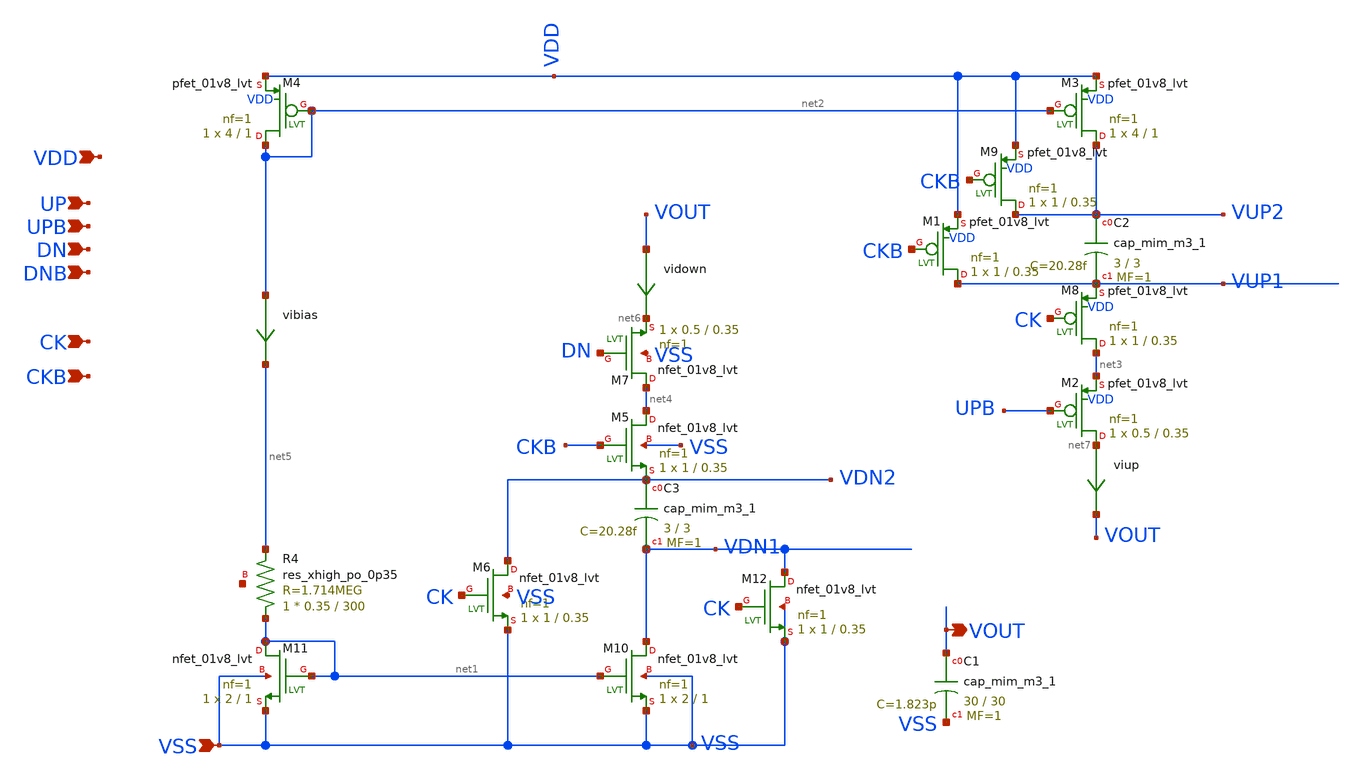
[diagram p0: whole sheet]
** sch_path: xschem/pll_cp_charlie.sch
**.subckt pll_cp_charlie VOUT VSS UP DNB CK CKB VDD DN UPB
*.opin VOUT
*.ipin VSS
*.ipin UP
*.ipin DNB
*.ipin CK
*.ipin CKB
*.ipin VDD
*.ipin DN
*.ipin UPB
XM5 net4 CKB VDN2 VSS sky130_fd_pr__nfet_01v8_lvt L=0.35 W=1 nf=1 ad='int((nf+1)/2) * W/nf * 0.29' as='int((nf+2)/2) * W/nf * 0.29'
+ pd='2*int((nf+1)/2) * (W/nf + 0.29)' ps='2*int((nf+2)/2) * (W/nf + 0.29)' nrd='0.29 / W' nrs='0.29 / W'
+ sa=0 sb=0 sd=0 mult=1 m=1
XM10 VDN1 net1 VSS VSS sky130_fd_pr__nfet_01v8_lvt L=1 W=2 nf=1 ad='int((nf+1)/2) * W/nf * 0.29' as='int((nf+2)/2) * W/nf * 0.29'
+ pd='2*int((nf+1)/2) * (W/nf + 0.29)' ps='2*int((nf+2)/2) * (W/nf + 0.29)' nrd='0.29 / W' nrs='0.29 / W'
+ sa=0 sb=0 sd=0 mult=1 m=1
vidown VOUT net6 0
.save i(vidown)
XM2 net7 UPB net3 VDD sky130_fd_pr__pfet_01v8_lvt L=0.35 W=0.5 nf=1 ad='int((nf+1)/2) * W/nf * 0.29'
+ as='int((nf+2)/2) * W/nf * 0.29' pd='2*int((nf+1)/2) * (W/nf + 0.29)' ps='2*int((nf+2)/2) * (W/nf + 0.29)'
+ nrd='0.29 / W' nrs='0.29 / W' sa=0 sb=0 sd=0 mult=1 m=1
XC1 VOUT VSS sky130_fd_pr__cap_mim_m3_1 W=30 L=30 MF=1 m=1
XM11 net1 net1 VSS VSS sky130_fd_pr__nfet_01v8_lvt L=1 W=2 nf=1 ad='int((nf+1)/2) * W/nf * 0.29' as='int((nf+2)/2) * W/nf * 0.29'
+ pd='2*int((nf+1)/2) * (W/nf + 0.29)' ps='2*int((nf+2)/2) * (W/nf + 0.29)' nrd='0.29 / W' nrs='0.29 / W'
+ sa=0 sb=0 sd=0 mult=1 m=1
XR4 net1 net5 net8 sky130_fd_pr__res_xhigh_po_0p35 L=300 mult=1 m=1
XM3 VUP2 net2 VDD VDD sky130_fd_pr__pfet_01v8_lvt L=1 W=4 nf=1 ad='int((nf+1)/2) * W/nf * 0.29' as='int((nf+2)/2) * W/nf * 0.29'
+ pd='2*int((nf+1)/2) * (W/nf + 0.29)' ps='2*int((nf+2)/2) * (W/nf + 0.29)' nrd='0.29 / W' nrs='0.29 / W'
+ sa=0 sb=0 sd=0 mult=1 m=1
XM4 net2 net2 VDD VDD sky130_fd_pr__pfet_01v8_lvt L=1 W=4 nf=1 ad='int((nf+1)/2) * W/nf * 0.29' as='int((nf+2)/2) * W/nf * 0.29'
+ pd='2*int((nf+1)/2) * (W/nf + 0.29)' ps='2*int((nf+2)/2) * (W/nf + 0.29)' nrd='0.29 / W' nrs='0.29 / W'
+ sa=0 sb=0 sd=0 mult=1 m=1
viup net7 VOUT 0
.save i(viup)
XM6 VDN2 CK VSS VSS sky130_fd_pr__nfet_01v8_lvt L=0.35 W=1 nf=1 ad='int((nf+1)/2) * W/nf * 0.29' as='int((nf+2)/2) * W/nf * 0.29'
+ pd='2*int((nf+1)/2) * (W/nf + 0.29)' ps='2*int((nf+2)/2) * (W/nf + 0.29)' nrd='0.29 / W' nrs='0.29 / W'
+ sa=0 sb=0 sd=0 mult=1 m=1
XM7 net4 DN net6 VSS sky130_fd_pr__nfet_01v8_lvt L=0.35 W=0.5 nf=1 ad='int((nf+1)/2) * W/nf * 0.29' as='int((nf+2)/2) * W/nf * 0.29'
+ pd='2*int((nf+1)/2) * (W/nf + 0.29)' ps='2*int((nf+2)/2) * (W/nf + 0.29)' nrd='0.29 / W' nrs='0.29 / W'
+ sa=0 sb=0 sd=0 mult=1 m=1
XM1 VUP1 CKB VDD VDD sky130_fd_pr__pfet_01v8_lvt L=0.35 W=1 nf=1 ad='int((nf+1)/2) * W/nf * 0.29' as='int((nf+2)/2) * W/nf * 0.29'
+ pd='2*int((nf+1)/2) * (W/nf + 0.29)' ps='2*int((nf+2)/2) * (W/nf + 0.29)' nrd='0.29 / W' nrs='0.29 / W'
+ sa=0 sb=0 sd=0 mult=1 m=1
XM8 net3 CK VUP1 VDD sky130_fd_pr__pfet_01v8_lvt L=0.35 W=1 nf=1 ad='int((nf+1)/2) * W/nf * 0.29' as='int((nf+2)/2) * W/nf * 0.29'
+ pd='2*int((nf+1)/2) * (W/nf + 0.29)' ps='2*int((nf+2)/2) * (W/nf + 0.29)' nrd='0.29 / W' nrs='0.29 / W'
+ sa=0 sb=0 sd=0 mult=1 m=1
vibias net2 net5 0
.save i(vibias)
XM9 VUP2 CKB VDD VDD sky130_fd_pr__pfet_01v8_lvt L=0.35 W=1 nf=1 ad='int((nf+1)/2) * W/nf * 0.29' as='int((nf+2)/2) * W/nf * 0.29'
+ pd='2*int((nf+1)/2) * (W/nf + 0.29)' ps='2*int((nf+2)/2) * (W/nf + 0.29)' nrd='0.29 / W' nrs='0.29 / W'
+ sa=0 sb=0 sd=0 mult=1 m=1
XM12 VDN1 CK VSS VSS sky130_fd_pr__nfet_01v8_lvt L=0.35 W=1 nf=1 ad='int((nf+1)/2) * W/nf * 0.29' as='int((nf+2)/2) * W/nf * 0.29'
+ pd='2*int((nf+1)/2) * (W/nf + 0.29)' ps='2*int((nf+2)/2) * (W/nf + 0.29)' nrd='0.29 / W' nrs='0.29 / W'
+ sa=0 sb=0 sd=0 mult=1 m=1
XC3 VDN2 VDN1 sky130_fd_pr__cap_mim_m3_1 W=3 L=3 MF=1 m=1
XC2 VUP2 VUP1 sky130_fd_pr__cap_mim_m3_1 W=3 L=3 MF=1 m=1
**.ends
.end
